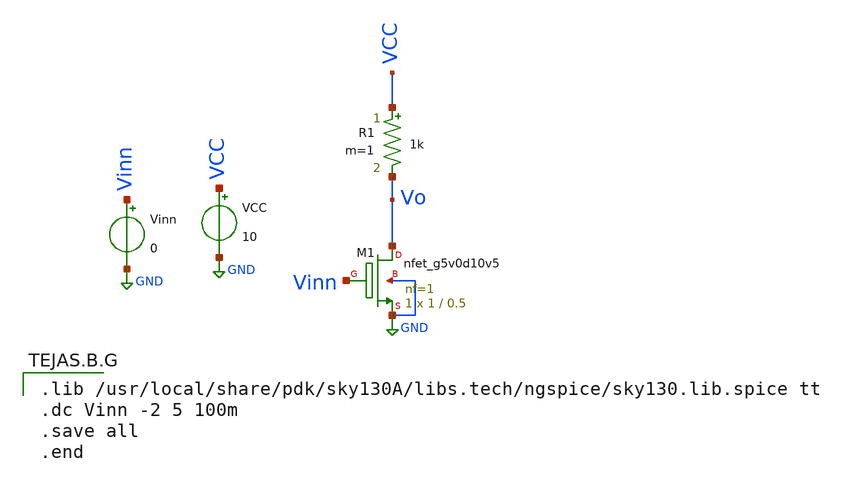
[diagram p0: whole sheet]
** sch_path: Schematic Simulation/threshold_calculating_schematics/nmoss_threshold.sch
**.subckt nmoss_threshold
VCC VCC GND 10
R1 VCC Vo 1k m=1
Vinn Vinn GND 0
XM1 Vo Vinn GND GND sky130_fd_pr__nfet_g5v0d10v5 L=0.5 W=1 nf=1 ad='int((nf+1)/2) * W/nf * 0.29' as='int((nf+2)/2) * W/nf * 0.29'
+ pd='2*int((nf+1)/2) * (W/nf + 0.29)' ps='2*int((nf+2)/2) * (W/nf + 0.29)' nrd='0.29 / W' nrs='0.29 / W'
+ sa=0 sb=0 sd=0 mult=1 m=1
**** begin user architecture code

.lib /usr/local/share/pdk/sky130A/libs.tech/ngspice/sky130.lib.spice tt
.dc Vinn -2 5 100m
.save all
.end

**** end user architecture code
**.ends
.GLOBAL GND
.end
